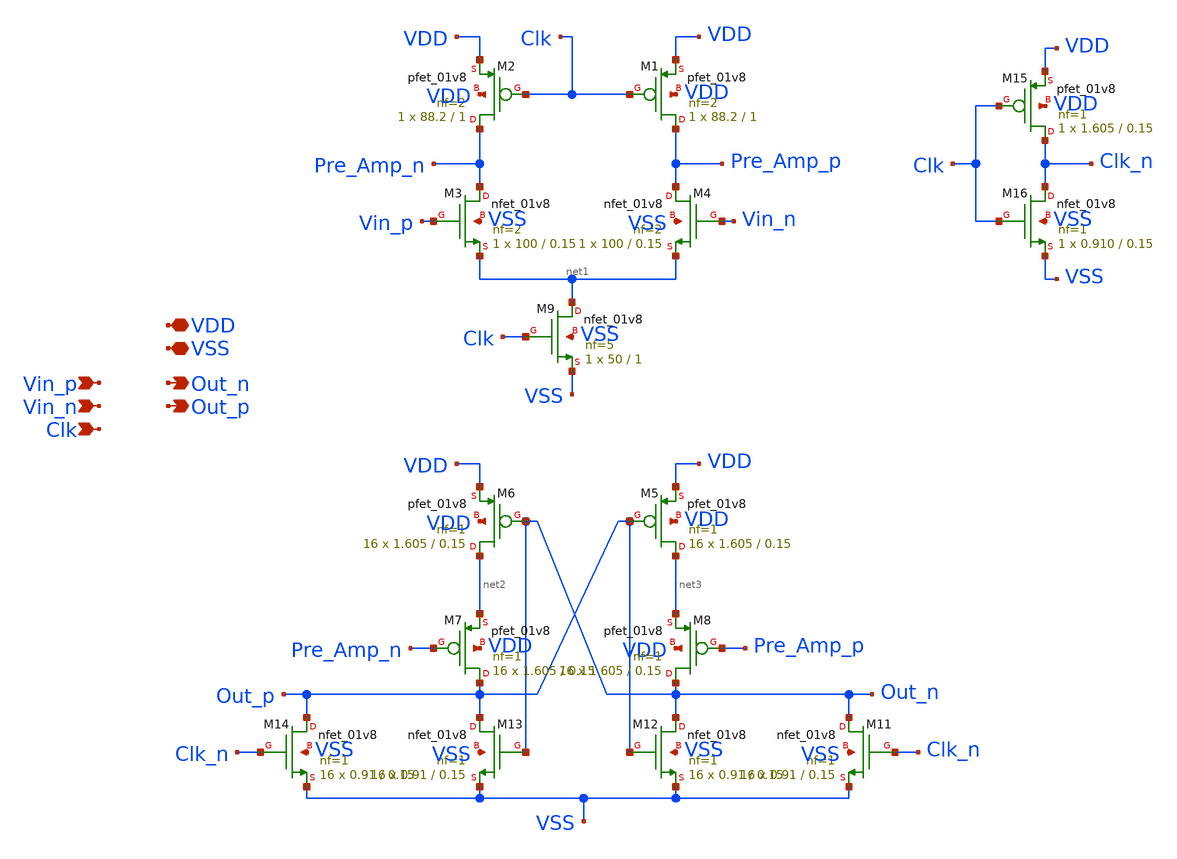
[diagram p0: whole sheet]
** sch_path: xschem/src/comparator/comparator.sch
**.subckt comparator VDD VSS Vin_p Out_n Vin_n Out_p Clk
*.iopin VDD
*.iopin VSS
*.ipin Vin_p
*.opin Out_n
*.ipin Vin_n
*.opin Out_p
*.ipin Clk
XM1 Pre_Amp_p Clk VDD VDD sky130_fd_pr__pfet_01v8 L=1 W=88.2 nf=2 ad='int((nf+1)/2) * W/nf * 0.29' as='int((nf+2)/2) * W/nf * 0.29'
+ pd='2*int((nf+1)/2) * (W/nf + 0.29)' ps='2*int((nf+2)/2) * (W/nf + 0.29)' nrd='0.29 / W' nrs='0.29 / W'
+ sa=0 sb=0 sd=0 mult=1 m=1
XM2 Pre_Amp_n Clk VDD VDD sky130_fd_pr__pfet_01v8 L=1 W=88.2 nf=2 ad='int((nf+1)/2) * W/nf * 0.29' as='int((nf+2)/2) * W/nf * 0.29'
+ pd='2*int((nf+1)/2) * (W/nf + 0.29)' ps='2*int((nf+2)/2) * (W/nf + 0.29)' nrd='0.29 / W' nrs='0.29 / W'
+ sa=0 sb=0 sd=0 mult=1 m=1
XM3 Pre_Amp_n Vin_p net1 VSS sky130_fd_pr__nfet_01v8 L=0.15 W=100 nf=2 ad='int((nf+1)/2) * W/nf * 0.29'
+ as='int((nf+2)/2) * W/nf * 0.29' pd='2*int((nf+1)/2) * (W/nf + 0.29)' ps='2*int((nf+2)/2) * (W/nf + 0.29)'
+ nrd='0.29 / W' nrs='0.29 / W' sa=0 sb=0 sd=0 mult=1 m=1
XM4 Pre_Amp_p Vin_n net1 VSS sky130_fd_pr__nfet_01v8 L=0.15 W=100 nf=2 ad='int((nf+1)/2) * W/nf * 0.29'
+ as='int((nf+2)/2) * W/nf * 0.29' pd='2*int((nf+1)/2) * (W/nf + 0.29)' ps='2*int((nf+2)/2) * (W/nf + 0.29)'
+ nrd='0.29 / W' nrs='0.29 / W' sa=0 sb=0 sd=0 mult=1 m=1
XM5 net3 Out_p VDD VDD sky130_fd_pr__pfet_01v8 L=0.15 W=1.605 nf=1 ad='int((nf+1)/2) * W/nf * 0.29' as='int((nf+2)/2) * W/nf * 0.29'
+ pd='2*int((nf+1)/2) * (W/nf + 0.29)' ps='2*int((nf+2)/2) * (W/nf + 0.29)' nrd='0.29 / W' nrs='0.29 / W'
+ sa=0 sb=0 sd=0 mult=16 m=16
XM6 net2 Out_n VDD VDD sky130_fd_pr__pfet_01v8 L=0.15 W=1.605 nf=1 ad='int((nf+1)/2) * W/nf * 0.29' as='int((nf+2)/2) * W/nf * 0.29'
+ pd='2*int((nf+1)/2) * (W/nf + 0.29)' ps='2*int((nf+2)/2) * (W/nf + 0.29)' nrd='0.29 / W' nrs='0.29 / W'
+ sa=0 sb=0 sd=0 mult=16 m=16
XM9 net1 Clk VSS VSS sky130_fd_pr__nfet_01v8 L=1 W=50 nf=5 ad='int((nf+1)/2) * W/nf * 0.29' as='int((nf+2)/2) * W/nf * 0.29'
+ pd='2*int((nf+1)/2) * (W/nf + 0.29)' ps='2*int((nf+2)/2) * (W/nf + 0.29)' nrd='0.29 / W' nrs='0.29 / W'
+ sa=0 sb=0 sd=0 mult=1 m=1
XM11 Out_n Clk_n VSS VSS sky130_fd_pr__nfet_01v8 L=0.15 W=0.91 nf=1 ad='int((nf+1)/2) * W/nf * 0.29'
+ as='int((nf+2)/2) * W/nf * 0.29' pd='2*int((nf+1)/2) * (W/nf + 0.29)' ps='2*int((nf+2)/2) * (W/nf + 0.29)'
+ nrd='0.29 / W' nrs='0.29 / W' sa=0 sb=0 sd=0 mult=16 m=16
XM12 Out_n Out_p VSS VSS sky130_fd_pr__nfet_01v8 L=0.15 W=0.91 nf=1 ad='int((nf+1)/2) * W/nf * 0.29'
+ as='int((nf+2)/2) * W/nf * 0.29' pd='2*int((nf+1)/2) * (W/nf + 0.29)' ps='2*int((nf+2)/2) * (W/nf + 0.29)'
+ nrd='0.29 / W' nrs='0.29 / W' sa=0 sb=0 sd=0 mult=16 m=16
XM13 Out_p Out_n VSS VSS sky130_fd_pr__nfet_01v8 L=0.15 W=0.91 nf=1 ad='int((nf+1)/2) * W/nf * 0.29'
+ as='int((nf+2)/2) * W/nf * 0.29' pd='2*int((nf+1)/2) * (W/nf + 0.29)' ps='2*int((nf+2)/2) * (W/nf + 0.29)'
+ nrd='0.29 / W' nrs='0.29 / W' sa=0 sb=0 sd=0 mult=16 m=16
XM14 Out_p Clk_n VSS VSS sky130_fd_pr__nfet_01v8 L=0.15 W=0.91 nf=1 ad='int((nf+1)/2) * W/nf * 0.29'
+ as='int((nf+2)/2) * W/nf * 0.29' pd='2*int((nf+1)/2) * (W/nf + 0.29)' ps='2*int((nf+2)/2) * (W/nf + 0.29)'
+ nrd='0.29 / W' nrs='0.29 / W' sa=0 sb=0 sd=0 mult=16 m=16
XM15 Clk_n Clk VDD VDD sky130_fd_pr__pfet_01v8 L=0.15 W=1.605 nf=1 ad='int((nf+1)/2) * W/nf * 0.29' as='int((nf+2)/2) * W/nf * 0.29'
+ pd='2*int((nf+1)/2) * (W/nf + 0.29)' ps='2*int((nf+2)/2) * (W/nf + 0.29)' nrd='0.29 / W' nrs='0.29 / W'
+ sa=0 sb=0 sd=0 mult=1 m=1
XM16 Clk_n Clk VSS VSS sky130_fd_pr__nfet_01v8 L=0.15 W=0.910 nf=1 ad='int((nf+1)/2) * W/nf * 0.29' as='int((nf+2)/2) * W/nf * 0.29'
+ pd='2*int((nf+1)/2) * (W/nf + 0.29)' ps='2*int((nf+2)/2) * (W/nf + 0.29)' nrd='0.29 / W' nrs='0.29 / W'
+ sa=0 sb=0 sd=0 mult=1 m=1
XM7 Out_p Pre_Amp_n net2 VDD sky130_fd_pr__pfet_01v8 L=0.15 W=1.605 nf=1 ad='int((nf+1)/2) * W/nf * 0.29'
+ as='int((nf+2)/2) * W/nf * 0.29' pd='2*int((nf+1)/2) * (W/nf + 0.29)' ps='2*int((nf+2)/2) * (W/nf + 0.29)'
+ nrd='0.29 / W' nrs='0.29 / W' sa=0 sb=0 sd=0 mult=16 m=16
XM8 Out_n Pre_Amp_p net3 VDD sky130_fd_pr__pfet_01v8 L=0.15 W=1.605 nf=1 ad='int((nf+1)/2) * W/nf * 0.29'
+ as='int((nf+2)/2) * W/nf * 0.29' pd='2*int((nf+1)/2) * (W/nf + 0.29)' ps='2*int((nf+2)/2) * (W/nf + 0.29)'
+ nrd='0.29 / W' nrs='0.29 / W' sa=0 sb=0 sd=0 mult=16 m=16
**.ends
.end
